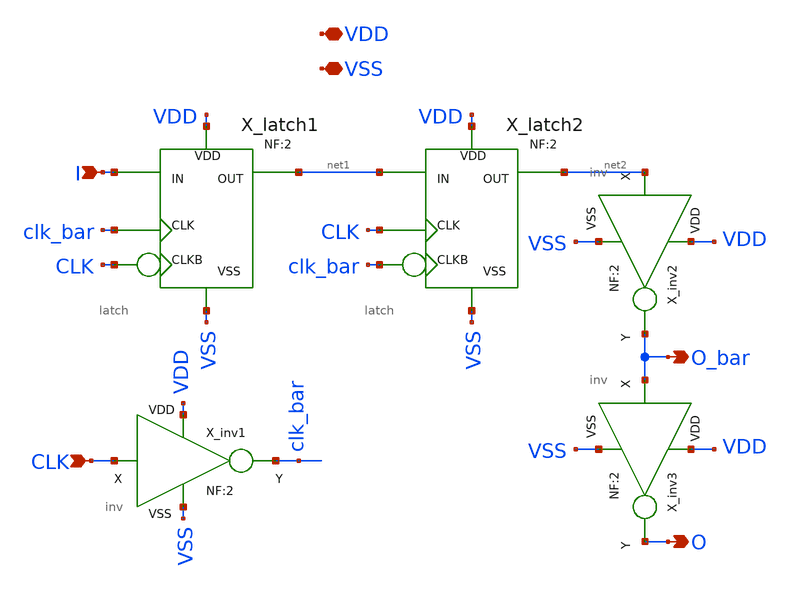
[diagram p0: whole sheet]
** sch_path: xschem_lib/DFFRAM_full_custom/DFF.sch
**.subckt DFF VDD VSS I CLK O O_bar
*.iopin VDD
*.iopin VSS
*.ipin I
*.ipin CLK
*.opin O
*.opin O_bar
X_latch1 I clk_bar CLK VSS VDD net1 latch NF=2
X_latch2 net1 CLK clk_bar VSS VDD net2 latch NF=2
X_inv1 CLK VDD VSS clk_bar inv NF=2
X_inv2 net2 VDD VSS O_bar inv NF=2
X_inv3 O_bar VDD VSS O inv NF=2
**.ends
.end
